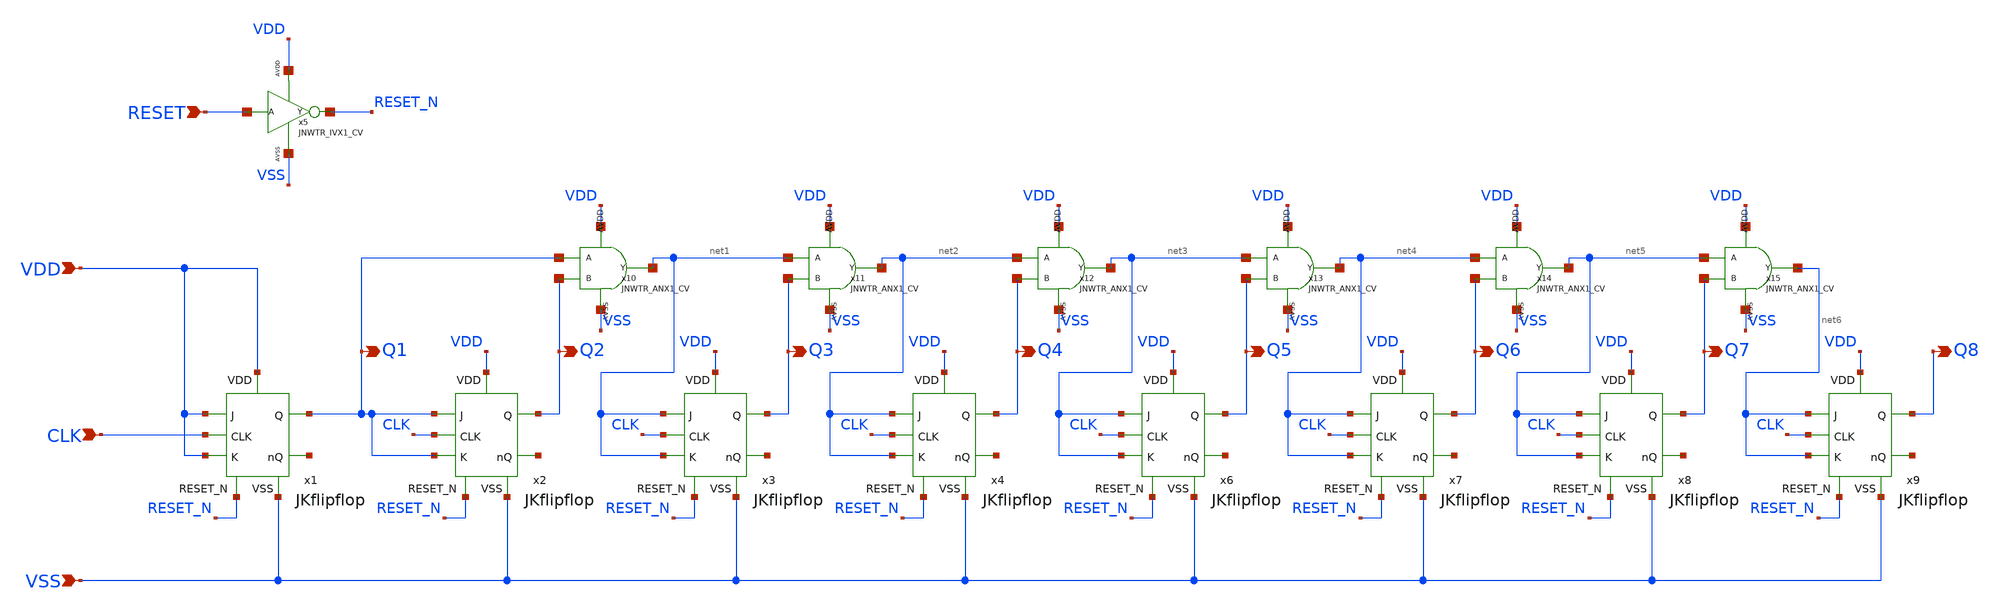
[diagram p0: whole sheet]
** sch_path: design/JNW_GR05_SKY130A/synCounter_8bit.sch
**.subckt synCounter_8bit VDD VSS CLK RESET Q2 Q1 Q3 Q4 Q5 Q6 Q7 Q8
*.ipin VDD
*.ipin VSS
*.ipin CLK
*.ipin RESET
*.opin Q2
*.opin Q1
*.opin Q3
*.opin Q4
*.opin Q5
*.opin Q6
*.opin Q7
*.opin Q8
x5 RESET RESET_N VDD VSS JNWTR_IVX1_CV
x1 VDD VDD Q1 CLK net7 VDD VSS RESET_N JKflipflop
x2 VDD Q1 Q2 CLK net8 Q1 VSS RESET_N JKflipflop
x3 VDD net1 Q3 CLK net9 net1 VSS RESET_N JKflipflop
x4 VDD net2 Q4 CLK net10 net2 VSS RESET_N JKflipflop
x6 VDD net3 Q5 CLK net11 net3 VSS RESET_N JKflipflop
x7 VDD net4 Q6 CLK net12 net4 VSS RESET_N JKflipflop
x8 VDD net5 Q7 CLK net13 net5 VSS RESET_N JKflipflop
x9 VDD net6 Q8 CLK net14 net6 VSS RESET_N JKflipflop
x10 Q1 Q2 net1 VDD VSS JNWTR_ANX1_CV xoffset=0 yoffset=0 angle=0 M=1
x11 net1 Q3 net2 VDD VSS JNWTR_ANX1_CV xoffset=0 yoffset=0 angle=0 M=1
x12 net2 Q4 net3 VDD VSS JNWTR_ANX1_CV xoffset=0 yoffset=0 angle=0 M=1
x13 net3 Q5 net4 VDD VSS JNWTR_ANX1_CV xoffset=0 yoffset=0 angle=0 M=1
x14 net4 Q6 net5 VDD VSS JNWTR_ANX1_CV xoffset=0 yoffset=0 angle=0 M=1
x15 net5 Q7 net6 VDD VSS JNWTR_ANX1_CV xoffset=0 yoffset=0 angle=0 M=1
**.ends
.end
